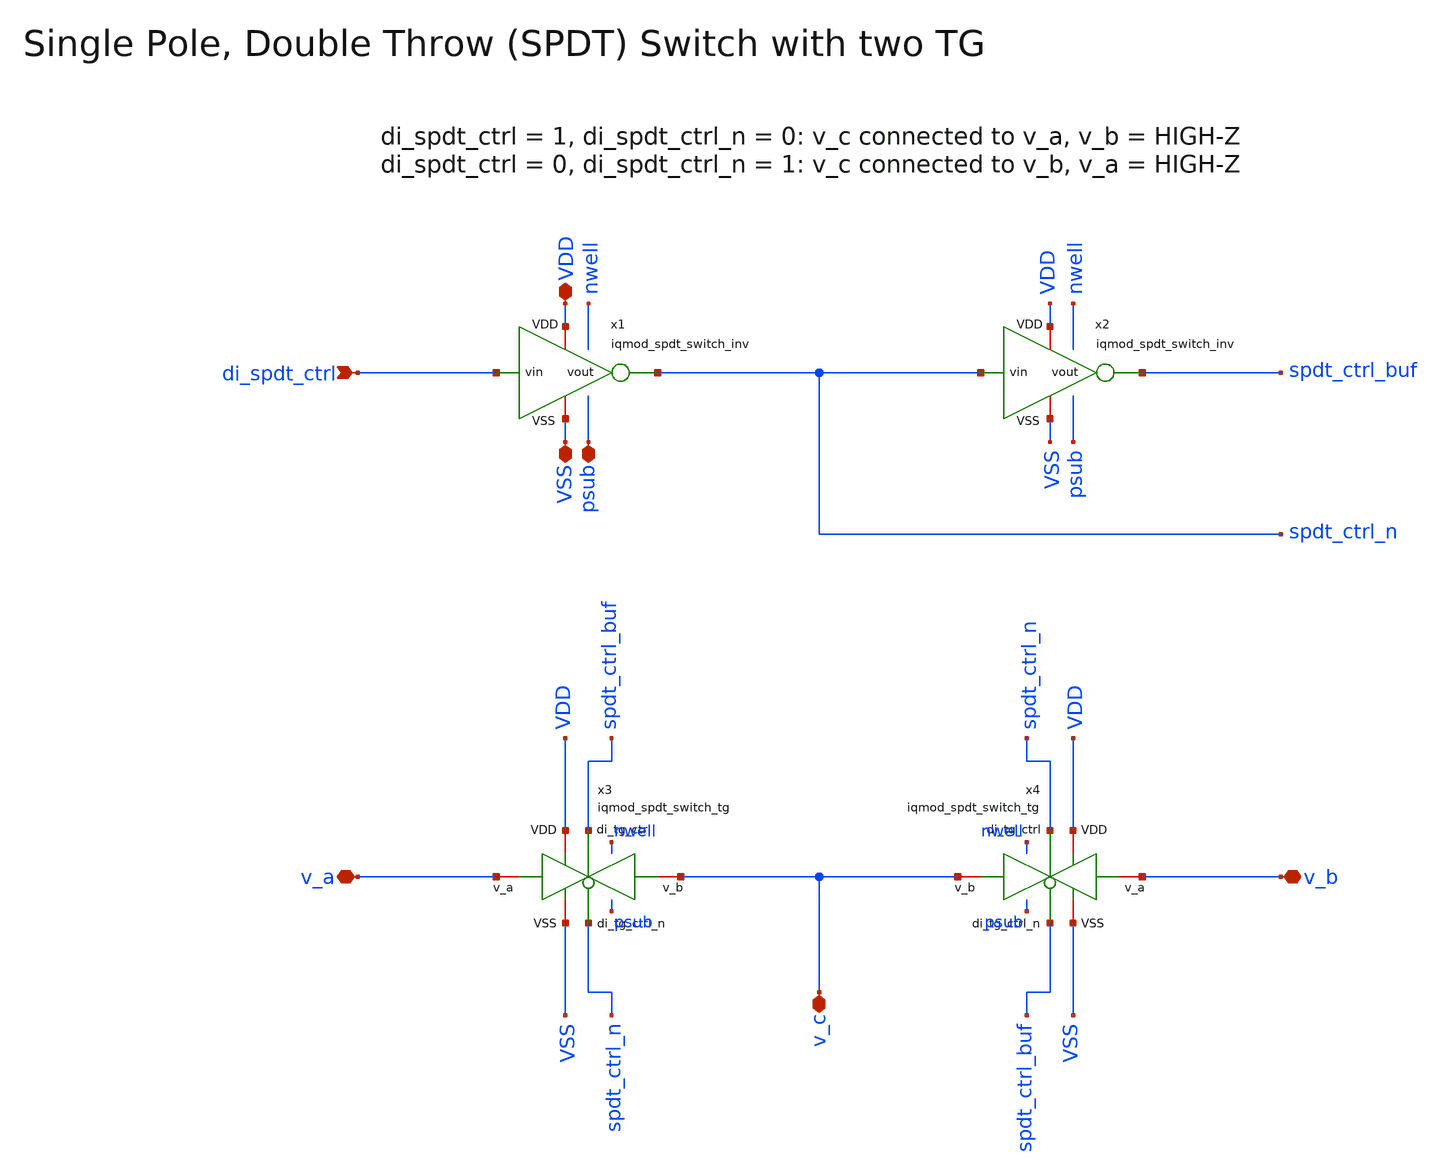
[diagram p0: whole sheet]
** sch_path: ihp130/macros/iqmod/xschem/iqmod_spdt_switch.sch
**.subckt iqmod_spdt_switch v_a v_b v_c VDD VSS di_spdt_ctrl psub
*.iopin v_a
*.iopin v_b
*.iopin v_c
*.iopin VDD
*.iopin VSS
*.ipin di_spdt_ctrl
*.iopin psub
x1 VDD di_spdt_ctrl spdt_ctrl_n VSS iqmod_spdt_switch_inv
x2 VDD spdt_ctrl_n spdt_ctrl_buf VSS iqmod_spdt_switch_inv
x3 VDD spdt_ctrl_buf VSS v_c v_a spdt_ctrl_n iqmod_spdt_switch_tg
x4 VDD spdt_ctrl_n VSS v_c v_b spdt_ctrl_buf iqmod_spdt_switch_tg
**.ends
.end
